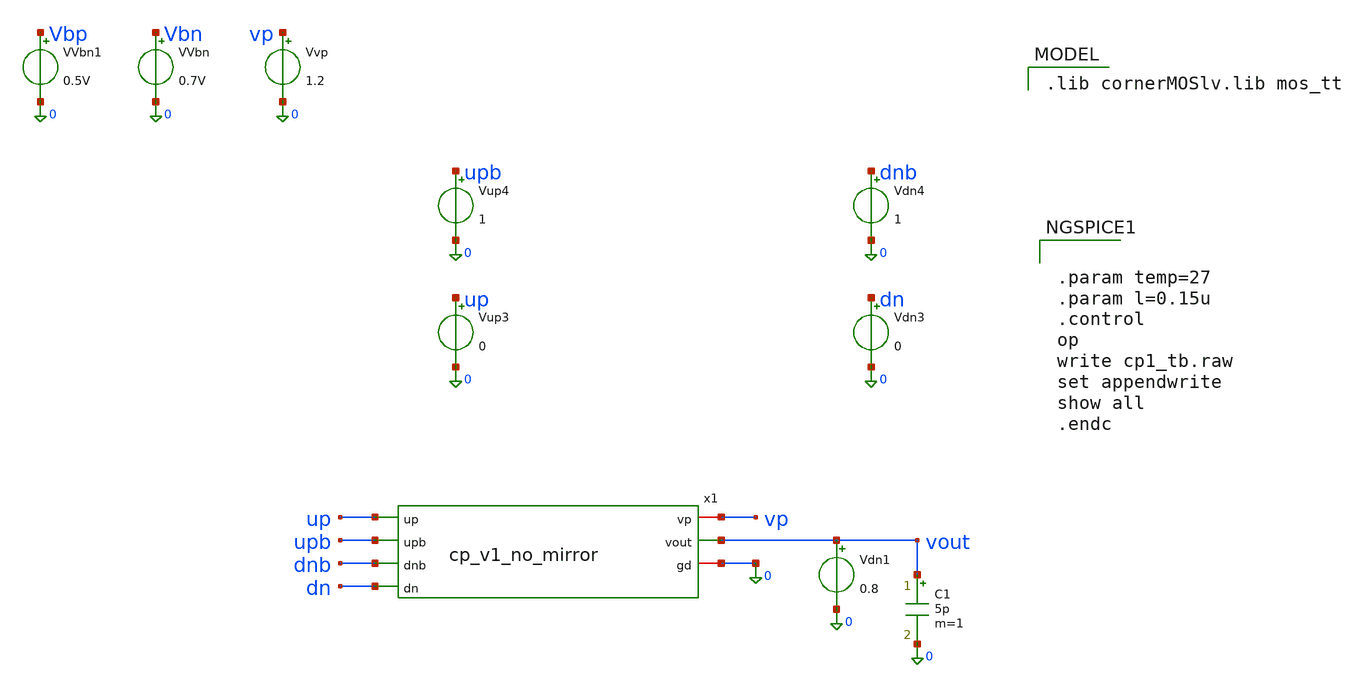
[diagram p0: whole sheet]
** sch_path: PLL0663-main/schematic/xschem/charge_pump/old_sch/cp_v1_tb_2.sch
**.subckt cp_v1_tb_2
Vvp vp 0 1.2
VVbn Vbn 0 0.7V
C1 vout 0 5p m=1
VVbn1 Vbp 0 0.5V
Vup3 up 0 0
Vdn3 dn 0 0
Vup4 upb 0 1
Vdn4 dnb 0 1
x1 vp up upb vout dnb dn 0 cp_v1_no_mirror
Vdn1 vout 0 0.8
**** begin user architecture code
 .lib cornerMOSlv.lib mos_tt



.param temp=27
.param l=0.15u
.control
op
write cp1_tb.raw
set appendwrite
show all
.endc


**** end user architecture code
**.ends
.end
